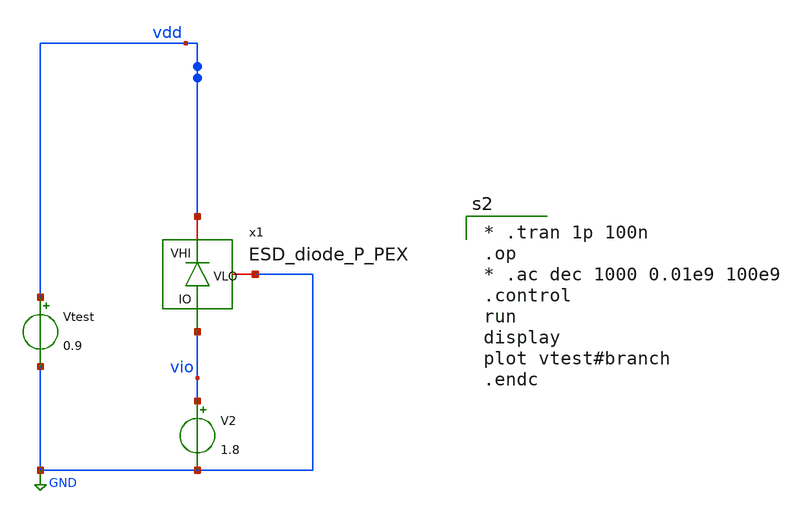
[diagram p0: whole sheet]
** sch_path: xschem/ESD_tb.sch
**.subckt ESD_tb
x1 vdd GND vio ESD_diode_P_PEX
Vtest vdd GND 0.9
V2 vio GND 1.8
**** begin user architecture code
.lib $::SKYWATER_MODELS/sky130.lib.spice tt
.include /home/al/openmpw/pdk_1/sky130B/libs.ref/sky130_fd_sc_hd/spice/sky130_fd_sc_hd.spice


* .tran 1p 100n
.op
* .ac dec 1000 0.01e9 100e9
.control
run
display
plot vtest#branch
.endc


**** end user architecture code
**.ends

* expanding   symbol:  ESD_diode_P_PEX.sym # of pins=3
** sym_path: xschem/ESD_diode_P_PEX.sym
** sch_path: xschem/ESD_diode_P_PEX.sch
.subckt ESD_diode_P_PEX VHI VLO IO
*.iopin VHI
*.iopin VLO
*.iopin IO
**** begin user architecture code

D0 IO VHI sky130_fd_pr__diode_pd2nw_05v5 pj=2.2e+07u area=1e+13p
D1 IO VHI sky130_fd_pr__diode_pd2nw_05v5 pj=2.2e+07u area=1e+13p
D2 IO VHI sky130_fd_pr__diode_pd2nw_05v5 pj=2.2e+07u area=1e+13p
D3 IO VHI sky130_fd_pr__diode_pd2nw_05v5 pj=2.2e+07u area=1e+13p
C0 VHI IO 42.11fF
C1 VHI VLO 22.58fF


**** end user architecture code
.ends

.GLOBAL GND
.end
